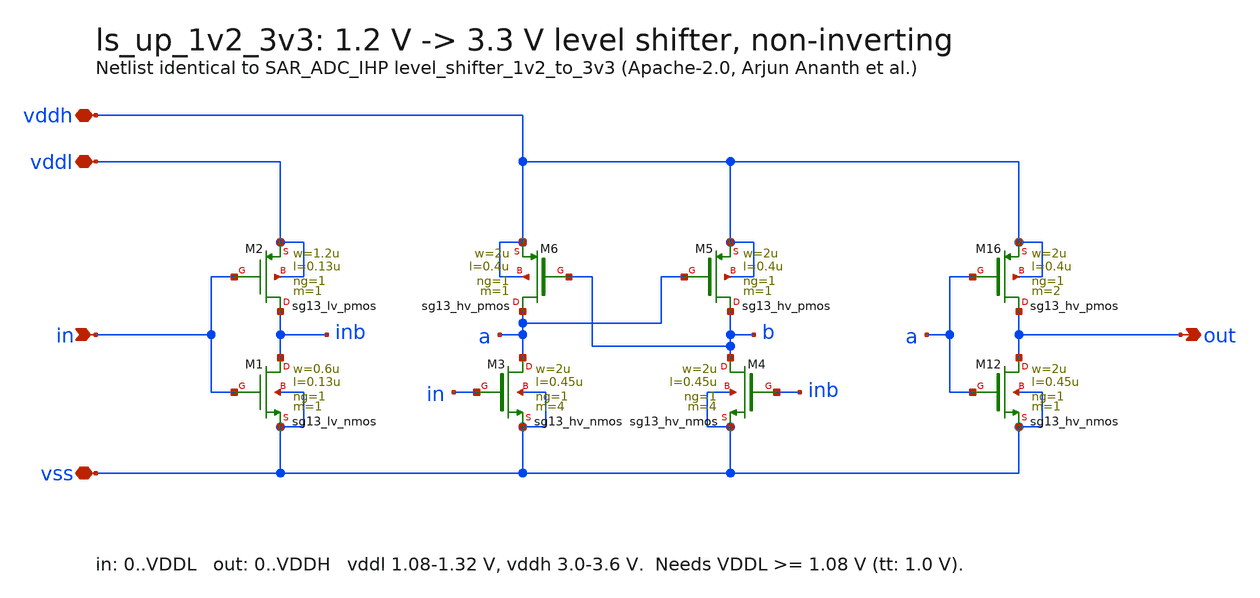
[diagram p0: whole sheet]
** sch_path: ls_pair/xschem/ls_up_1v2_3v3.sch
**.subckt ls_up_1v2_3v3 vss vddl vddh out in
*.iopin vss
*.iopin vddl
*.iopin vddh
*.opin out
*.ipin in
XM2 inb in vddl vddl sg13_lv_pmos w=1.2u l=0.13u ng=1 m=1 mm_ok=1
XM1 inb in vss vss sg13_lv_nmos w=0.6u l=0.13u ng=1 m=1 mm_ok=1
XM3 a in vss vss sg13_hv_nmos w=2u l=0.45u ng=1 m=4 mm_ok=1
XM6 a b vddh vddh sg13_hv_pmos w=2u l=0.4u ng=1 m=1 mm_ok=1
XM5 b a vddh vddh sg13_hv_pmos w=2u l=0.4u ng=1 m=1 mm_ok=1
XM4 b inb vss vss sg13_hv_nmos w=2u l=0.45u ng=1 m=4 mm_ok=1
XM16 out a vddh vddh sg13_hv_pmos w=2u l=0.4u ng=1 m=2 mm_ok=1
XM12 out a vss vss sg13_hv_nmos w=2u l=0.45u ng=1 m=1 mm_ok=1
**.ends
.end
